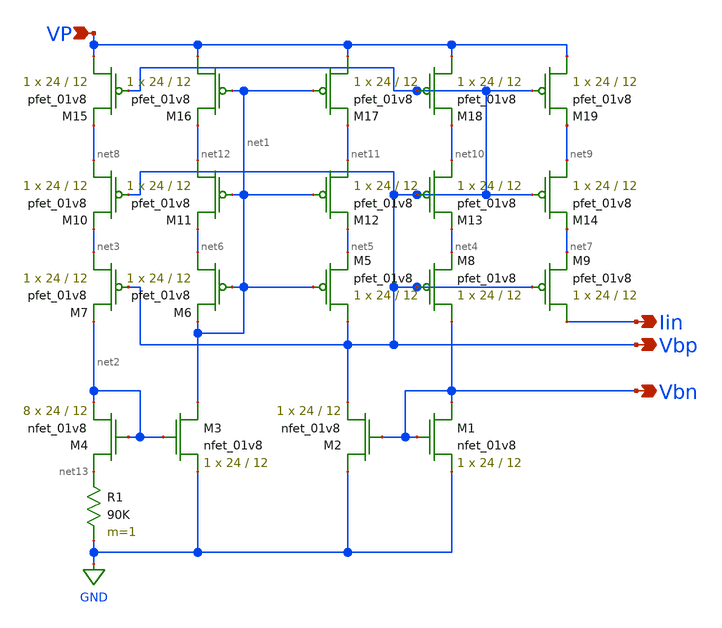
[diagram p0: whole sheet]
** sch_path: xschem/biasGen.sch
**.subckt biasGen Iin VP Vbp Vbn
*.opin Iin
*.ipin VP
*.opin Vbp
*.opin Vbn
XM1 Vbn Vbn GND GND sky130_fd_pr__nfet_01v8 L=12 W=24 nf=1 ad='int((nf+1)/2) * W/nf * 0.29' as='int((nf+2)/2) * W/nf * 0.29'
+ pd='2*int((nf+1)/2) * (W/nf + 0.29)' ps='2*int((nf+2)/2) * (W/nf + 0.29)' nrd='0.29 / W' nrs='0.29 / W'
+ sa=0 sb=0 sd=0 mult=1 m=1
XM2 GND Vbn Vbp GND sky130_fd_pr__nfet_01v8 L=12 W=24 nf=1 ad='int((nf+1)/2) * W/nf * 0.29' as='int((nf+2)/2) * W/nf * 0.29'
+ pd='2*int((nf+1)/2) * (W/nf + 0.29)' ps='2*int((nf+2)/2) * (W/nf + 0.29)' nrd='0.29 / W' nrs='0.29 / W'
+ sa=0 sb=0 sd=0 mult=1 m=1
XM3 net1 net2 GND GND sky130_fd_pr__nfet_01v8 L=12 W=24 nf=1 ad='int((nf+1)/2) * W/nf * 0.29' as='int((nf+2)/2) * W/nf * 0.29'
+ pd='2*int((nf+1)/2) * (W/nf + 0.29)' ps='2*int((nf+2)/2) * (W/nf + 0.29)' nrd='0.29 / W' nrs='0.29 / W'
+ sa=0 sb=0 sd=0 mult=1 m=1
XM4 net13 net2 net2 GND sky130_fd_pr__nfet_01v8 L=12 W=24 nf=1 ad='int((nf+1)/2) * W/nf * 0.29' as='int((nf+2)/2) * W/nf * 0.29'
+ pd='2*int((nf+1)/2) * (W/nf + 0.29)' ps='2*int((nf+2)/2) * (W/nf + 0.29)' nrd='0.29 / W' nrs='0.29 / W'
+ sa=0 sb=0 sd=0 mult=8 m=8
XM5 Vbp net1 net5 VDD sky130_fd_pr__pfet_01v8 L=12 W=24 nf=1 ad='int((nf+1)/2) * W/nf * 0.29' as='int((nf+2)/2) * W/nf * 0.29'
+ pd='2*int((nf+1)/2) * (W/nf + 0.29)' ps='2*int((nf+2)/2) * (W/nf + 0.29)' nrd='0.29 / W' nrs='0.29 / W'
+ sa=0 sb=0 sd=0 mult=1 m=1
XM6 net6 net1 net1 VDD sky130_fd_pr__pfet_01v8 L=12 W=24 nf=1 ad='int((nf+1)/2) * W/nf * 0.29' as='int((nf+2)/2) * W/nf * 0.29'
+ pd='2*int((nf+1)/2) * (W/nf + 0.29)' ps='2*int((nf+2)/2) * (W/nf + 0.29)' nrd='0.29 / W' nrs='0.29 / W'
+ sa=0 sb=0 sd=0 mult=1 m=1
XM7 net3 Vbp net2 VDD sky130_fd_pr__pfet_01v8 L=12 W=24 nf=1 ad='int((nf+1)/2) * W/nf * 0.29' as='int((nf+2)/2) * W/nf * 0.29'
+ pd='2*int((nf+1)/2) * (W/nf + 0.29)' ps='2*int((nf+2)/2) * (W/nf + 0.29)' nrd='0.29 / W' nrs='0.29 / W'
+ sa=0 sb=0 sd=0 mult=1 m=1
XM8 Vbn Vbp net4 VDD sky130_fd_pr__pfet_01v8 L=12 W=24 nf=1 ad='int((nf+1)/2) * W/nf * 0.29' as='int((nf+2)/2) * W/nf * 0.29'
+ pd='2*int((nf+1)/2) * (W/nf + 0.29)' ps='2*int((nf+2)/2) * (W/nf + 0.29)' nrd='0.29 / W' nrs='0.29 / W'
+ sa=0 sb=0 sd=0 mult=1 m=1
R1 net13 GND 90K m=1
XM9 Iin Vbp net7 VDD sky130_fd_pr__pfet_01v8 L=12 W=24 nf=1 ad='int((nf+1)/2) * W/nf * 0.29' as='int((nf+2)/2) * W/nf * 0.29'
+ pd='2*int((nf+1)/2) * (W/nf + 0.29)' ps='2*int((nf+2)/2) * (W/nf + 0.29)' nrd='0.29 / W' nrs='0.29 / W'
+ sa=0 sb=0 sd=0 mult=1 m=1
XM10 net8 Vbp net3 VDD sky130_fd_pr__pfet_01v8 L=12 W=24 nf=1 ad='int((nf+1)/2) * W/nf * 0.29' as='int((nf+2)/2) * W/nf * 0.29'
+ pd='2*int((nf+1)/2) * (W/nf + 0.29)' ps='2*int((nf+2)/2) * (W/nf + 0.29)' nrd='0.29 / W' nrs='0.29 / W'
+ sa=0 sb=0 sd=0 mult=1 m=1
XM11 net12 net1 net6 VDD sky130_fd_pr__pfet_01v8 L=12 W=24 nf=1 ad='int((nf+1)/2) * W/nf * 0.29' as='int((nf+2)/2) * W/nf * 0.29'
+ pd='2*int((nf+1)/2) * (W/nf + 0.29)' ps='2*int((nf+2)/2) * (W/nf + 0.29)' nrd='0.29 / W' nrs='0.29 / W'
+ sa=0 sb=0 sd=0 mult=1 m=1
XM12 net11 net1 net5 VDD sky130_fd_pr__pfet_01v8 L=12 W=24 nf=1 ad='int((nf+1)/2) * W/nf * 0.29' as='int((nf+2)/2) * W/nf * 0.29'
+ pd='2*int((nf+1)/2) * (W/nf + 0.29)' ps='2*int((nf+2)/2) * (W/nf + 0.29)' nrd='0.29 / W' nrs='0.29 / W'
+ sa=0 sb=0 sd=0 mult=1 m=1
XM13 net10 Vbp net4 VDD sky130_fd_pr__pfet_01v8 L=12 W=24 nf=1 ad='int((nf+1)/2) * W/nf * 0.29' as='int((nf+2)/2) * W/nf * 0.29'
+ pd='2*int((nf+1)/2) * (W/nf + 0.29)' ps='2*int((nf+2)/2) * (W/nf + 0.29)' nrd='0.29 / W' nrs='0.29 / W'
+ sa=0 sb=0 sd=0 mult=1 m=1
XM14 net9 Vbp net7 VDD sky130_fd_pr__pfet_01v8 L=12 W=24 nf=1 ad='int((nf+1)/2) * W/nf * 0.29' as='int((nf+2)/2) * W/nf * 0.29'
+ pd='2*int((nf+1)/2) * (W/nf + 0.29)' ps='2*int((nf+2)/2) * (W/nf + 0.29)' nrd='0.29 / W' nrs='0.29 / W'
+ sa=0 sb=0 sd=0 mult=1 m=1
XM15 VP Vbp net8 VDD sky130_fd_pr__pfet_01v8 L=12 W=24 nf=1 ad='int((nf+1)/2) * W/nf * 0.29' as='int((nf+2)/2) * W/nf * 0.29'
+ pd='2*int((nf+1)/2) * (W/nf + 0.29)' ps='2*int((nf+2)/2) * (W/nf + 0.29)' nrd='0.29 / W' nrs='0.29 / W'
+ sa=0 sb=0 sd=0 mult=1 m=1
XM16 VP net1 net12 VDD sky130_fd_pr__pfet_01v8 L=12 W=24 nf=1 ad='int((nf+1)/2) * W/nf * 0.29' as='int((nf+2)/2) * W/nf * 0.29'
+ pd='2*int((nf+1)/2) * (W/nf + 0.29)' ps='2*int((nf+2)/2) * (W/nf + 0.29)' nrd='0.29 / W' nrs='0.29 / W'
+ sa=0 sb=0 sd=0 mult=1 m=1
XM17 VP net1 net11 VDD sky130_fd_pr__pfet_01v8 L=12 W=24 nf=1 ad='int((nf+1)/2) * W/nf * 0.29' as='int((nf+2)/2) * W/nf * 0.29'
+ pd='2*int((nf+1)/2) * (W/nf + 0.29)' ps='2*int((nf+2)/2) * (W/nf + 0.29)' nrd='0.29 / W' nrs='0.29 / W'
+ sa=0 sb=0 sd=0 mult=1 m=1
XM18 VP Vbp net10 VDD sky130_fd_pr__pfet_01v8 L=12 W=24 nf=1 ad='int((nf+1)/2) * W/nf * 0.29' as='int((nf+2)/2) * W/nf * 0.29'
+ pd='2*int((nf+1)/2) * (W/nf + 0.29)' ps='2*int((nf+2)/2) * (W/nf + 0.29)' nrd='0.29 / W' nrs='0.29 / W'
+ sa=0 sb=0 sd=0 mult=1 m=1
XM19 VP Vbp net9 VDD sky130_fd_pr__pfet_01v8 L=12 W=24 nf=1 ad='int((nf+1)/2) * W/nf * 0.29' as='int((nf+2)/2) * W/nf * 0.29'
+ pd='2*int((nf+1)/2) * (W/nf + 0.29)' ps='2*int((nf+2)/2) * (W/nf + 0.29)' nrd='0.29 / W' nrs='0.29 / W'
+ sa=0 sb=0 sd=0 mult=1 m=1
**.ends
.GLOBAL GND
.end
